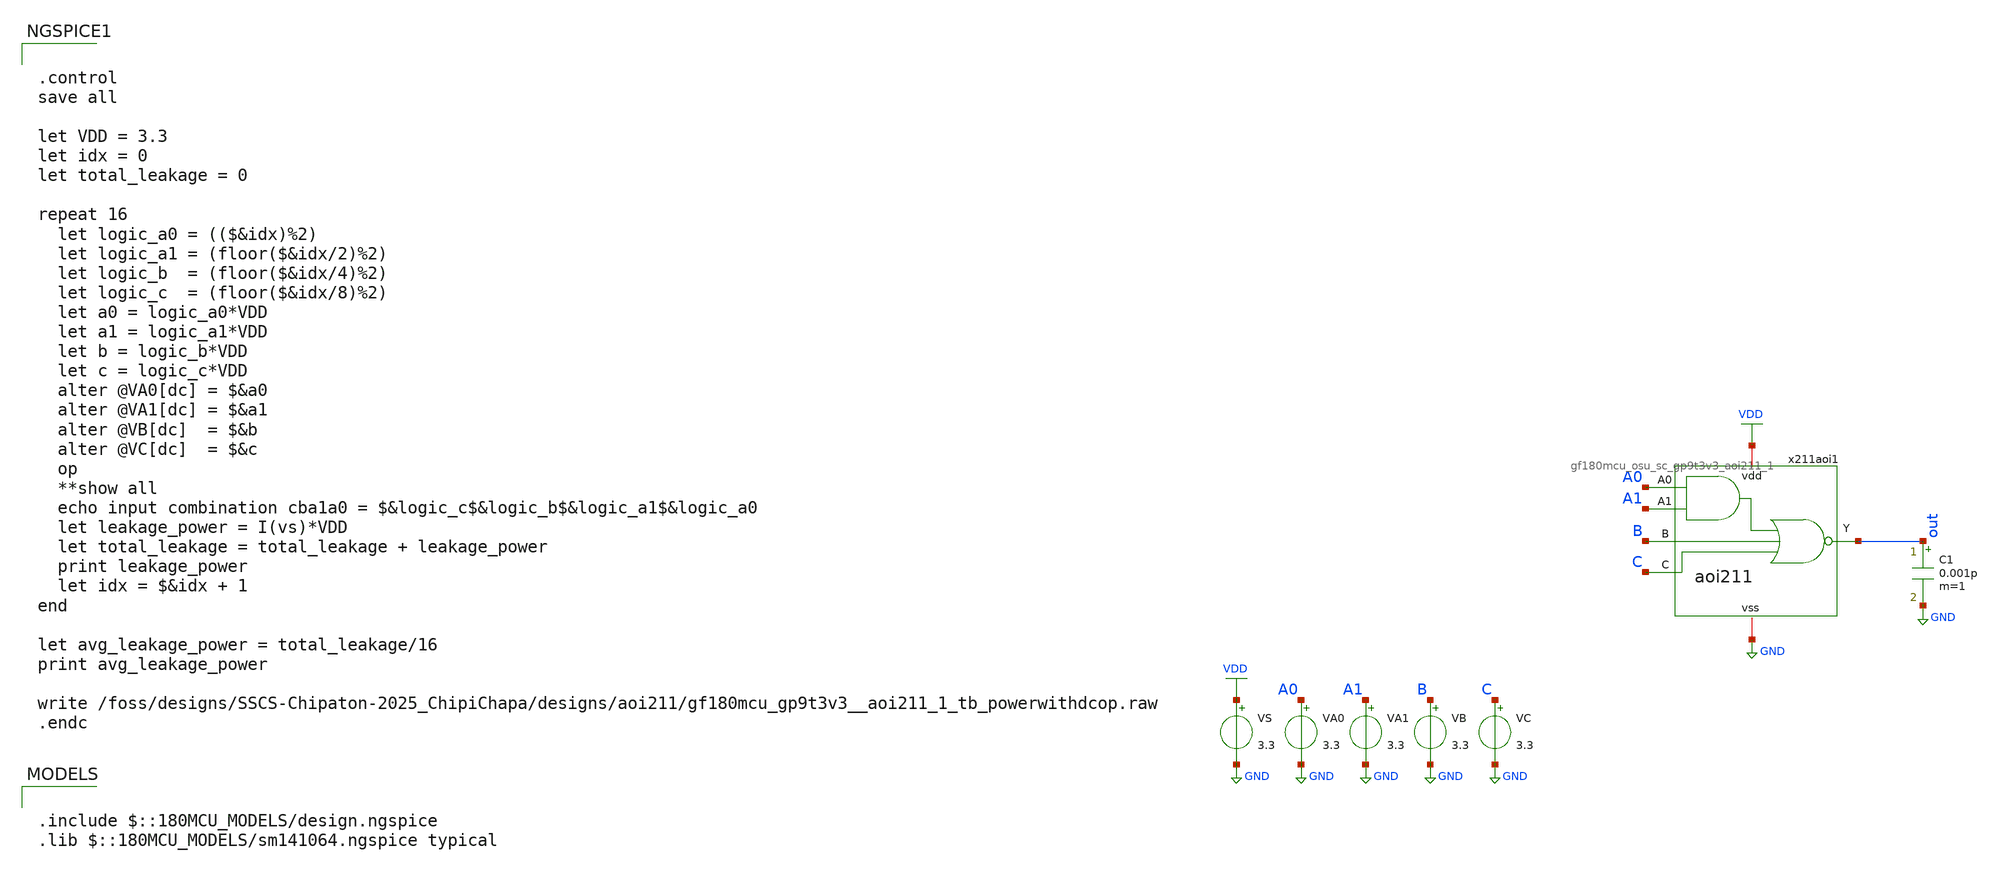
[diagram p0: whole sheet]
** sch_path: designs/aoi211/gf180mcu_osu_gp9t3v3_aoi211_1_tb_powerwithdcop.sch
**.subckt gf180mcu_osu_gp9t3v3_aoi211_1_tb_powerwithdcop
VA0 A0 GND 3.3
VA1 A1 GND 3.3
VB B GND 3.3
VC C GND 3.3
VS VDD GND 3.3
x211aoi1 VDD A1 A0 B C out GND gf180mcu_osu_sc_gp9t3v3_aoi211_1
C1 out GND 0.001p m=1
**** begin user architecture code


.control
save all

let VDD = 3.3
let idx = 0
let total_leakage = 0

repeat 16
  let logic_a0 = (($&idx)%2)
  let logic_a1 = (floor($&idx/2)%2)
  let logic_b  = (floor($&idx/4)%2)
  let logic_c  = (floor($&idx/8)%2)
  let a0 = logic_a0*VDD
  let a1 = logic_a1*VDD
  let b = logic_b*VDD
  let c = logic_c*VDD
  alter @VA0[dc] = $&a0
  alter @VA1[dc] = $&a1
  alter @VB[dc]  = $&b
  alter @VC[dc]  = $&c
  op
  **show all
  echo input combination cba1a0 = $&logic_c$&logic_b$&logic_a1$&logic_a0
  let leakage_power = I(vs)*VDD
  let total_leakage = total_leakage + leakage_power
  print leakage_power
  let idx = $&idx + 1
end

let avg_leakage_power = total_leakage/16
print avg_leakage_power

write
+ /foss/designs/SSCS-Chipaton-2025_ChipiChapa/designs/aoi211/gf180mcu_gp9t3v3__aoi211_1_tb_powerwithdcop.raw
.endc



.include $::180MCU_MODELS/design.ngspice
.lib $::180MCU_MODELS/sm141064.ngspice typical

**** end user architecture code
**.ends
.GLOBAL GND
.GLOBAL VDD
.end
